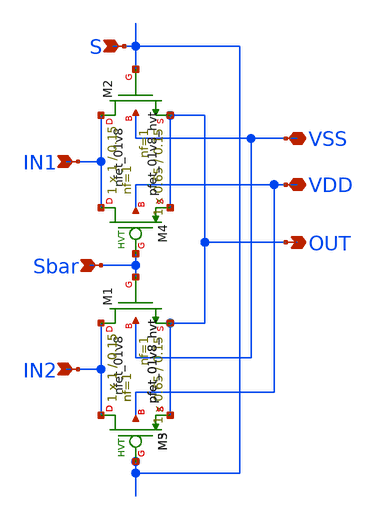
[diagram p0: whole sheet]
** sch_path: design/mux2-1.sch
**.subckt mux2-1 IN1 IN2 Sbar S OUT VSS VDD
*.ipin IN1
*.ipin IN2
*.ipin Sbar
*.ipin S
*.opin OUT
*.iopin VSS
*.iopin VDD
XM2 IN1 S OUT VSS sky130_fd_pr__nfet_01v8 L=0.15 W=0.65 nf=1 ad='int((nf+1)/2) * W/nf * 0.29' as='int((nf+2)/2) * W/nf * 0.29'
+ pd='2*int((nf+1)/2) * (W/nf + 0.29)' ps='2*int((nf+2)/2) * (W/nf + 0.29)' nrd='0.29 / W' nrs='0.29 / W'
+ sa=0 sb=0 sd=0 mult=1 m=1
XM1 IN2 Sbar OUT VSS sky130_fd_pr__nfet_01v8 L=0.15 W=0.65 nf=1 ad='int((nf+1)/2) * W/nf * 0.29' as='int((nf+2)/2) * W/nf * 0.29'
+ pd='2*int((nf+1)/2) * (W/nf + 0.29)' ps='2*int((nf+2)/2) * (W/nf + 0.29)' nrd='0.29 / W' nrs='0.29 / W'
+ sa=0 sb=0 sd=0 mult=1 m=1
XM3 IN2 S OUT VDD sky130_fd_pr__pfet_01v8_hvt L=0.15 W=1 nf=1 ad='int((nf+1)/2) * W/nf * 0.29' as='int((nf+2)/2) * W/nf * 0.29'
+ pd='2*int((nf+1)/2) * (W/nf + 0.29)' ps='2*int((nf+2)/2) * (W/nf + 0.29)' nrd='0.29 / W' nrs='0.29 / W'
+ sa=0 sb=0 sd=0 mult=1 m=1
XM4 IN1 Sbar OUT VDD sky130_fd_pr__pfet_01v8_hvt L=0.15 W=1 nf=1 ad='int((nf+1)/2) * W/nf * 0.29' as='int((nf+2)/2) * W/nf * 0.29'
+ pd='2*int((nf+1)/2) * (W/nf + 0.29)' ps='2*int((nf+2)/2) * (W/nf + 0.29)' nrd='0.29 / W' nrs='0.29 / W'
+ sa=0 sb=0 sd=0 mult=1 m=1
XM5 IN2 S OUT VDD sky130_fd_pr__pfet_01v8_hvt L=0.15 W=1 nf=1 ad='int((nf+1)/2) * W/nf * 0.29' as='int((nf+2)/2) * W/nf * 0.29'
+ pd='2*int((nf+1)/2) * (W/nf + 0.29)' ps='2*int((nf+2)/2) * (W/nf + 0.29)' nrd='0.29 / W' nrs='0.29 / W'
+ sa=0 sb=0 sd=0 mult=1 m=1
**.ends
.end
